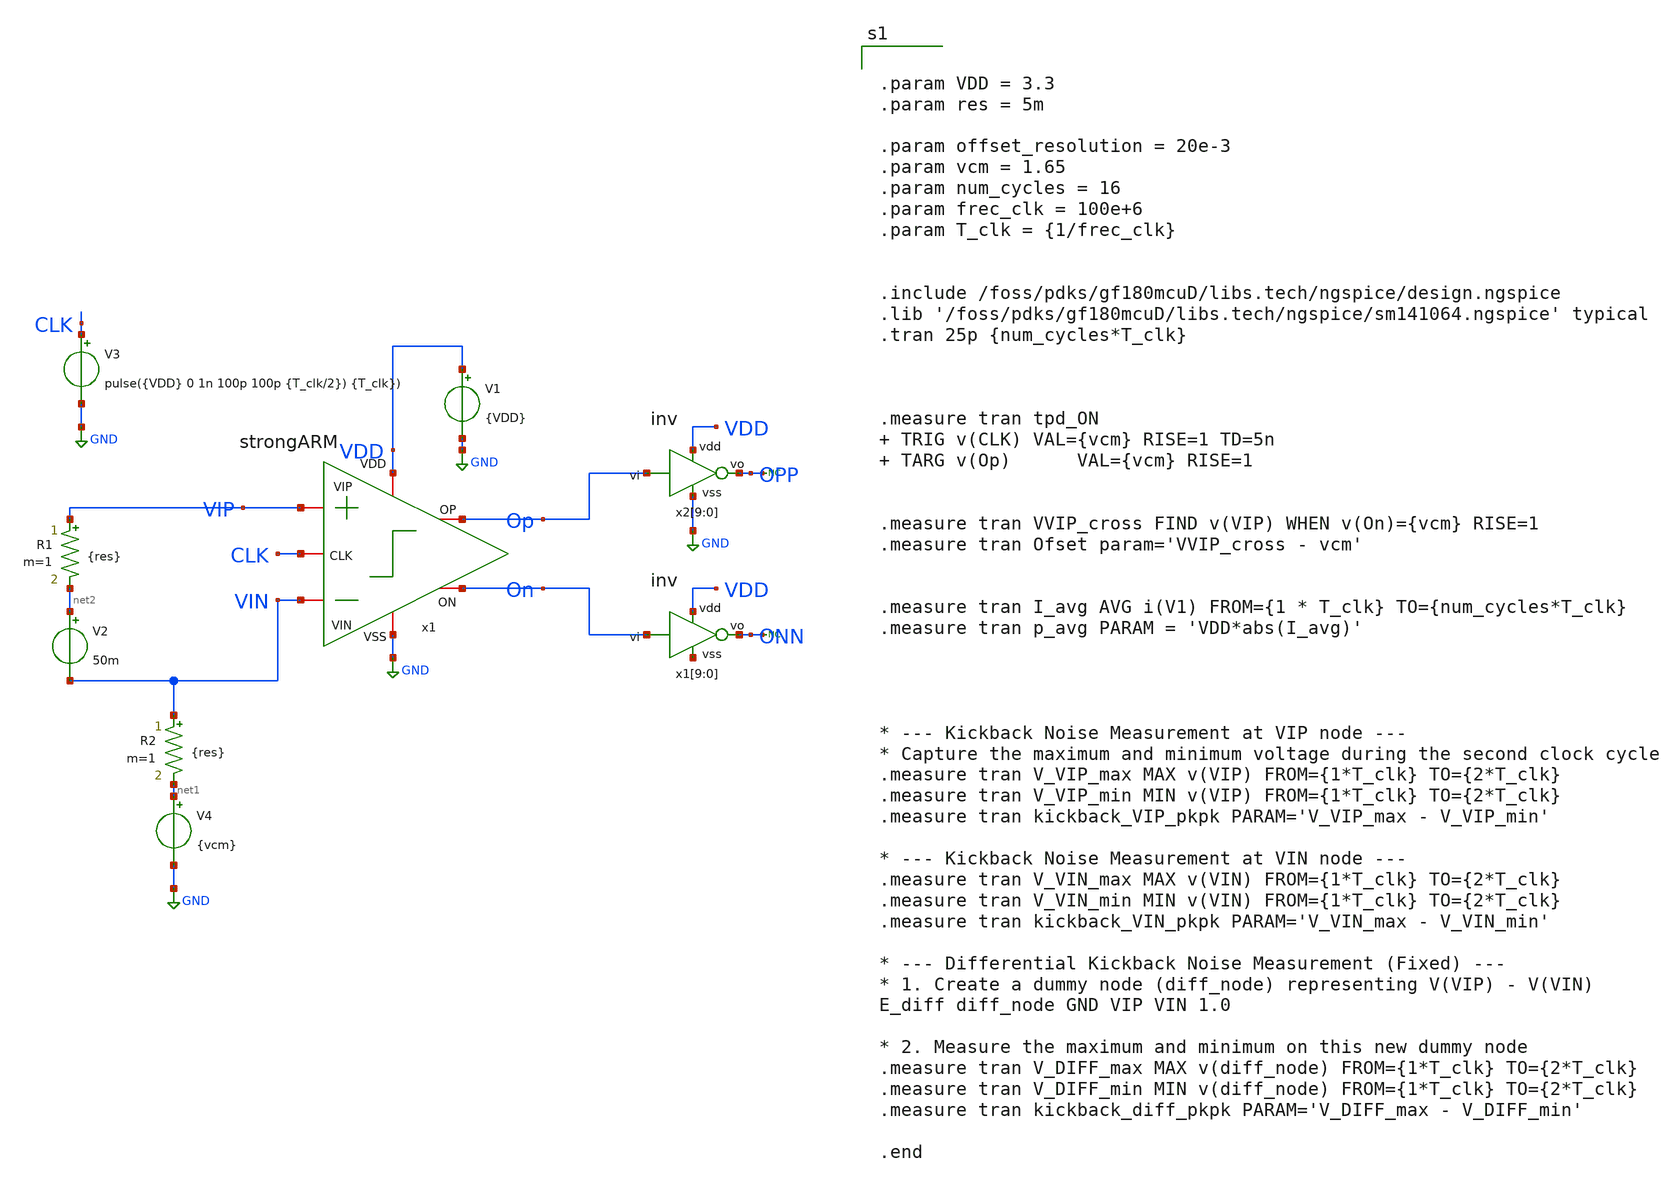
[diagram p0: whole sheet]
** sch_path: designs/sar_adc/comparator/Testbench/tb_Kickback_noise.sch
**.subckt tb_Kickback_noise
V1 VDD GND {VDD}
V2 net2 VIN 50m
V3 CLK GND pulse({VDD} 0 1n 100p 100p {T_clk/2}) {T_clk})
V4 net1 GND {vcm}
x1 VDD CLK On Op VIN VIP GND strongARM
x2[9] VDD Op OPP GND inv
x2[8] VDD Op OPP GND inv
x2[7] VDD Op OPP GND inv
x2[6] VDD Op OPP GND inv
x2[5] VDD Op OPP GND inv
x2[4] VDD Op OPP GND inv
x2[3] VDD Op OPP GND inv
x2[2] VDD Op OPP GND inv
x2[1] VDD Op OPP GND inv
x2[0] VDD Op OPP GND inv
x1[9] VDD On ONN net3[9] inv
x1[8] VDD On ONN net3[8] inv
x1[7] VDD On ONN net3[7] inv
x1[6] VDD On ONN net3[6] inv
x1[5] VDD On ONN net3[5] inv
x1[4] VDD On ONN net3[4] inv
x1[3] VDD On ONN net3[3] inv
x1[2] VDD On ONN net3[2] inv
x1[1] VDD On ONN net3[1] inv
x1[0] VDD On ONN net3[0] inv
* noconn ONN
* noconn OPP
R1 VIP net2 {res} m=1
R2 VIN net1 {res} m=1
**** begin user architecture code


.param VDD = 3.3
.param res = 5m

.param offset_resolution = 20e-3
.param vcm = 1.65
.param num_cycles = 16
.param frec_clk = 100e+6
.param T_clk = {1/frec_clk}


.include /foss/pdks/gf180mcuD/libs.tech/ngspice/design.ngspice
.lib '/foss/pdks/gf180mcuD/libs.tech/ngspice/sm141064.ngspice' typical
.tran 25p {num_cycles*T_clk}



.measure tran tpd_ON  TRIG v(CLK) VAL={vcm} RISE=1 TD=5n  TARG v(Op)      VAL={vcm} RISE=1


.measure tran VVIP_cross FIND v(VIP) WHEN v(On)={vcm} RISE=1
.measure tran Ofset param='VVIP_cross - vcm'


.measure tran I_avg AVG i(V1) FROM={1 * T_clk} TO={num_cycles*T_clk}
.measure tran p_avg PARAM = 'VDD*abs(I_avg)'




* --- Kickback Noise Measurement at VIP node ---
* Capture the maximum and minimum voltage during the second clock cycle
.measure tran V_VIP_max MAX v(VIP) FROM={1*T_clk} TO={2*T_clk}
.measure tran V_VIP_min MIN v(VIP) FROM={1*T_clk} TO={2*T_clk}
.measure tran kickback_VIP_pkpk PARAM='V_VIP_max - V_VIP_min'

* --- Kickback Noise Measurement at VIN node ---
.measure tran V_VIN_max MAX v(VIN) FROM={1*T_clk} TO={2*T_clk}
.measure tran V_VIN_min MIN v(VIN) FROM={1*T_clk} TO={2*T_clk}
.measure tran kickback_VIN_pkpk PARAM='V_VIN_max - V_VIN_min'

* --- Differential Kickback Noise Measurement (Fixed) ---
* 1. Create a dummy node (diff_node) representing V(VIP) - V(VIN)
E_diff diff_node GND VIP VIN 1.0

* 2. Measure the maximum and minimum on this new dummy node
.measure tran V_DIFF_max MAX v(diff_node) FROM={1*T_clk} TO={2*T_clk}
.measure tran V_DIFF_min MIN v(diff_node) FROM={1*T_clk} TO={2*T_clk}
.measure tran kickback_diff_pkpk PARAM='V_DIFF_max - V_DIFF_min'

.end


**** end user architecture code
**.ends
.GLOBAL GND
.end
